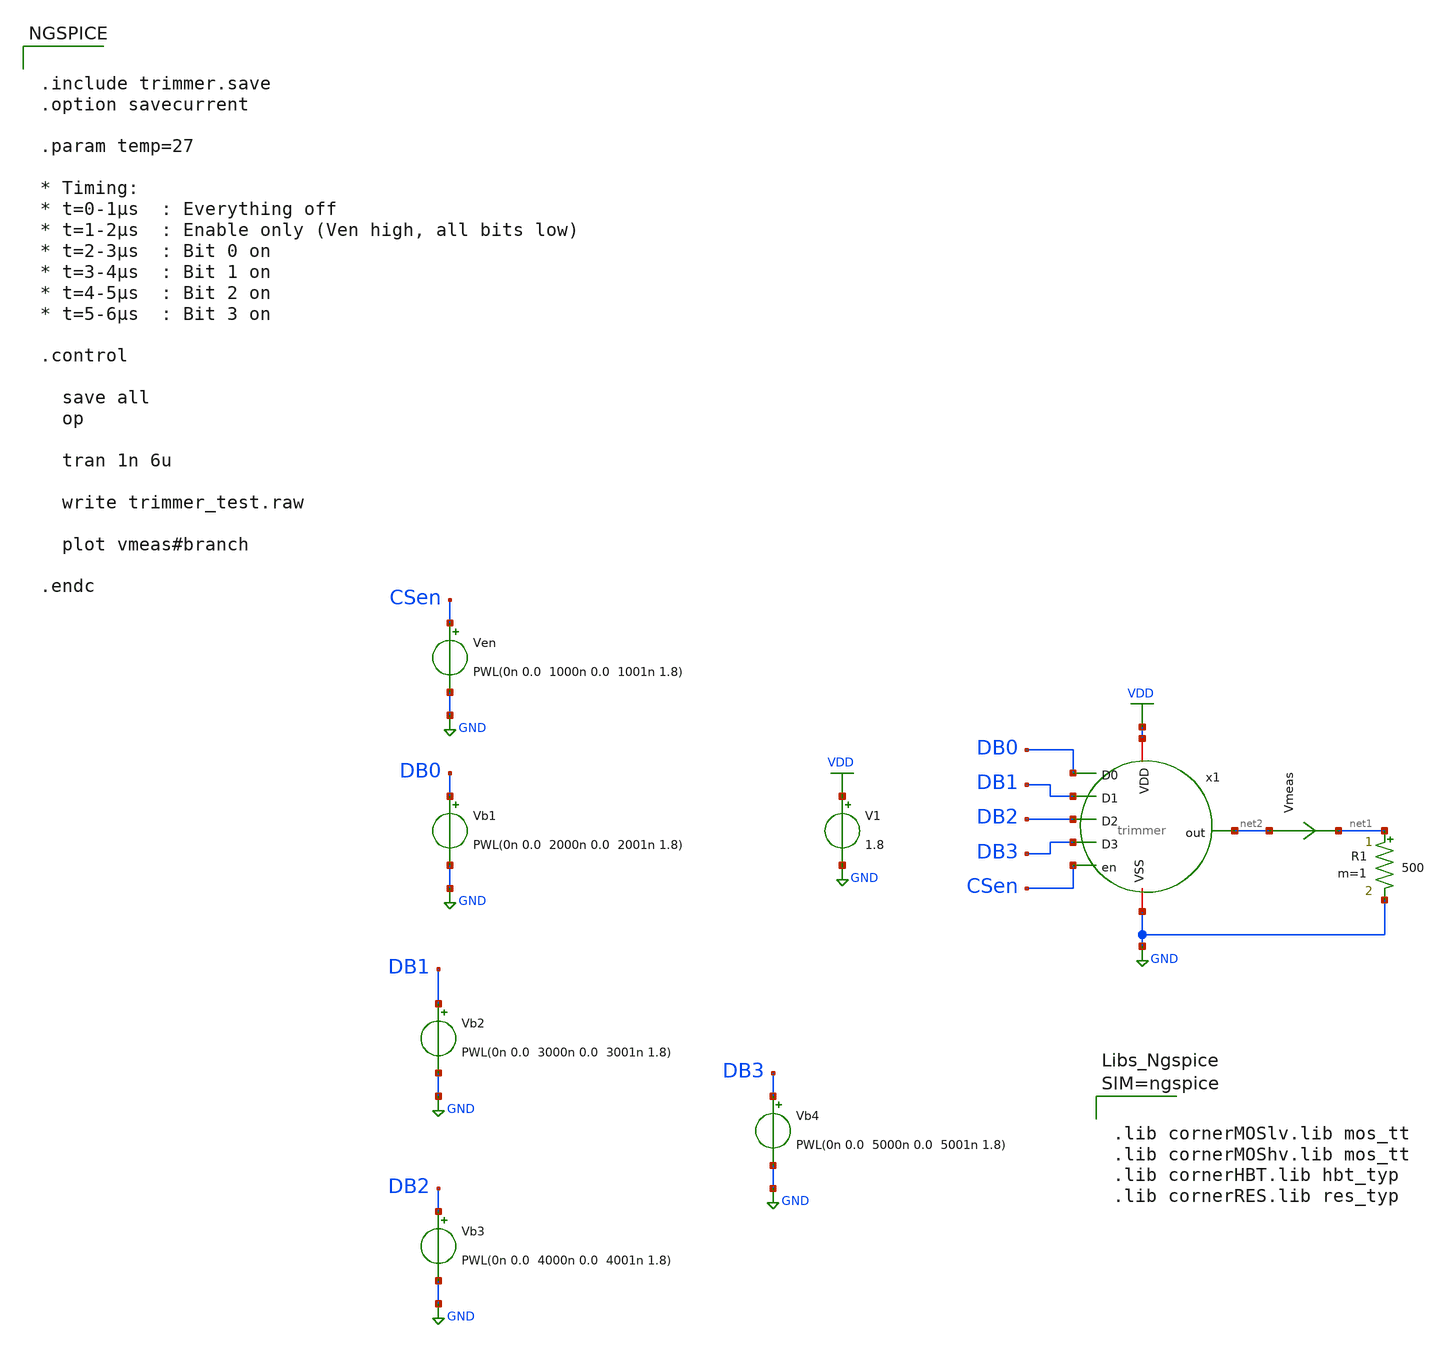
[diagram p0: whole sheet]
** sch_path: xschem/trimmer_test.sch
**.subckt trimmer_test
V1 VDD GND 1.8
Ven CSen GND PWL(0n 0.0 1000n 0.0 1001n 1.8)
Vb1 DB0 GND PWL(0n 0.0 2000n 0.0 2001n 1.8)
Vb2 DB1 GND PWL(0n 0.0 3000n 0.0 3001n 1.8)
Vb3 DB2 GND PWL(0n 0.0 4000n 0.0 4001n 1.8)
Vb4 DB3 GND PWL(0n 0.0 5000n 0.0 5001n 1.8)
x1 DB0 DB1 DB2 DB3 VDD GND CSen net2 trimmer
R1 net1 GND 500 m=1
Vmeas net2 net1 0
.save i(vmeas)
**** begin user architecture code


.include trimmer.save
.option savecurrent

.param temp=27

* Timing:
* t=0-1µs  : Everything off
* t=1-2µs  : Enable only (Ven high, all bits low)
* t=2-3µs  : Bit 0 on
* t=3-4µs  : Bit 1 on
* t=4-5µs  : Bit 2 on
* t=5-6µs  : Bit 3 on

.control

  save all
  op

  tran 1n 6u

  write trimmer_test.raw

  plot vmeas#branch

.endc





.lib cornerMOSlv.lib mos_tt
.lib cornerMOShv.lib mos_tt
.lib cornerHBT.lib hbt_typ
.lib cornerRES.lib res_typ



**** end user architecture code
**.ends

* expanding   symbol:  trimmer.sym # of pins=8
** sym_path: trimmer.sym
** sch_path: trimmer.sch
.subckt trimmer D0 D1 D2 D3 VDD VSS en out
*.ipin en
*.ipin D0
*.ipin D1
*.ipin D2
*.ipin D3
*.opin out
*.iopin VDD
*.iopin VSS
XMP1 net1 net1 net12 VDD sg13_lv_pmos w=0.28u l=8.0u ng=1 m=1 mm_ok=1
XMP2 vstart vstart net1 VDD sg13_lv_pmos w=0.28u l=8.0u ng=1 m=1 mm_ok=1
XMN2 net3 vstart VSS VSS sg13_lv_nmos w=0.28u l=8.0u ng=1 m=1 mm_ok=1
XMN1 vstart vstart VSS VSS sg13_lv_nmos w=0.28u l=8.0u ng=1 m=1 mm_ok=1
XMP3 net2 vbp net11 VDD sg13_lv_pmos w=2.0u l=2.0u ng=2 m=1 mm_ok=1
XMP4 net3 vbp_casc net2 VDD sg13_lv_pmos w=2.0u l=0.28u ng=1 m=2 mm_ok=1
XMP5 net4 vbp net10 VDD sg13_lv_pmos w=2.0u l=2.0u ng=1 m=2 mm_ok=1
XMP6 net6 vbp_casc net4 VDD sg13_lv_pmos w=2.0u l=0.28u ng=1 m=2 mm_ok=1
XMP7 net5 vbp net9 VDD sg13_lv_pmos w=2.0u l=2.0u ng=1 m=2 mm_ok=1
XMP8 vbp vbp_casc net5 VDD sg13_lv_pmos w=2.0u l=0.28u ng=1 m=2 mm_ok=1
XMP9 net6 net3 VDD VDD sg13_lv_pmos w=0.28u l=8.0u ng=1 m=1 mm_ok=1
XMN3 net6 net6 VSS VSS sg13_lv_nmos w=2.0u l=2.0u ng=1 m=1 mm_ok=1
XMN4 vbp_casc net6 net7 VSS sg13_lv_nmos w=2.0u l=2.0u ng=1 m=4 mm_ok=1
XR1 vbp vbp_casc sub! rppd w=0.5e-6 l=389e-6 m=1 b=0 mm_ok=1
XR2 net7 VSS sub! rhigh w=0.5e-6 l=152.5e-6 m=1 b=0 mm_ok=1
XMP10 net13 vbp net14 VDD sg13_lv_pmos w=2.0u l=2.0u ng=1 m=2 mm_ok=1
XMP11 out vbp_casc net13 VDD sg13_lv_pmos w=2.0u l=0.28u ng=1 m=2 mm_ok=1
XMP16 vbp_casc enMon VDD VDD sg13_lv_pmos w=2.0u l=0.28u ng=1 m=1 mm_ok=1
XMP17 net9 net8 VDD VDD sg13_lv_pmos w=2.0u l=0.28u ng=1 m=2 mm_ok=1
XMP18 net10 net8 VDD VDD sg13_lv_pmos w=2.0u l=0.28u ng=1 m=2 mm_ok=1
XMP19 net12 net8 VDD VDD sg13_lv_pmos w=2.0u l=0.28u ng=1 m=1 mm_ok=1
XMP20 net11 net8 VDD VDD sg13_lv_pmos w=2.0u l=0.28u ng=1 m=1 mm_ok=1
XMN5 vstart net8 VSS VSS sg13_lv_nmos w=2u l=0.28u ng=1 m=1 mm_ok=1
XMN6 net6 net8 VSS VSS sg13_lv_nmos w=2u l=0.28u ng=1 m=1 mm_ok=1
XMP12 net14 net15 VDD VDD sg13_lv_pmos w=2.0u l=0.28u ng=1 m=2 mm_ok=1
XMP13 net16 vbp net17 VDD sg13_lv_pmos w=2.0u l=2.0u ng=1 m=4 mm_ok=1
XMP14 out vbp_casc net16 VDD sg13_lv_pmos w=2.0u l=0.28u ng=1 m=4 mm_ok=1
XMP15 net17 net18 VDD VDD sg13_lv_pmos w=2.0u l=0.28u ng=1 m=2 mm_ok=1
XMP21 net19 vbp net20 VDD sg13_lv_pmos w=2.0u l=2.0u ng=1 m=8 mm_ok=1
XMP22 out vbp_casc net19 VDD sg13_lv_pmos w=2.0u l=0.28u ng=1 m=8 mm_ok=1
XMP23 net20 net21 VDD VDD sg13_lv_pmos w=2.0u l=0.28u ng=1 m=2 mm_ok=1
XMP24 net22 vbp net23 VDD sg13_lv_pmos w=2.0u l=2.0u ng=1 m=16 mm_ok=1
XMP25 out vbp_casc net22 VDD sg13_lv_pmos w=2.0u l=0.28u ng=1 m=16 mm_ok=1
XMP26 net23 net24 VDD VDD sg13_lv_pmos w=2.0u l=0.28u ng=1 m=2 mm_ok=1
xinv6 net25 net26 net8 net27 inv
xinv3 net28 net29 net30 net31 inv
xinv7 net32 net33 net34 net35 inv
xinv8 net36 net37 net38 net39 inv
xinv9 net40 net41 net42 net43 inv
xinv1 net44 net45 net46 net47 inv
.ends


* expanding   symbol:  inv.sym # of pins=4
** sym_path: xschem/inv.sym
** sch_path: xschem/inv.sch
.subckt inv VDD in out VSS
*.iopin VDD
*.ipin in
*.iopin VSS
*.opin out
XM1 out in VSS VSS sg13_lv_nmos w=1.2u l=0.28u ng=1 m=1 mm_ok=1
XM2 out in VDD VDD sg13_lv_pmos w=2.4u l=0.28u ng=1 m=1 mm_ok=1
.ends

.GLOBAL GND
.GLOBAL VDD
.end
